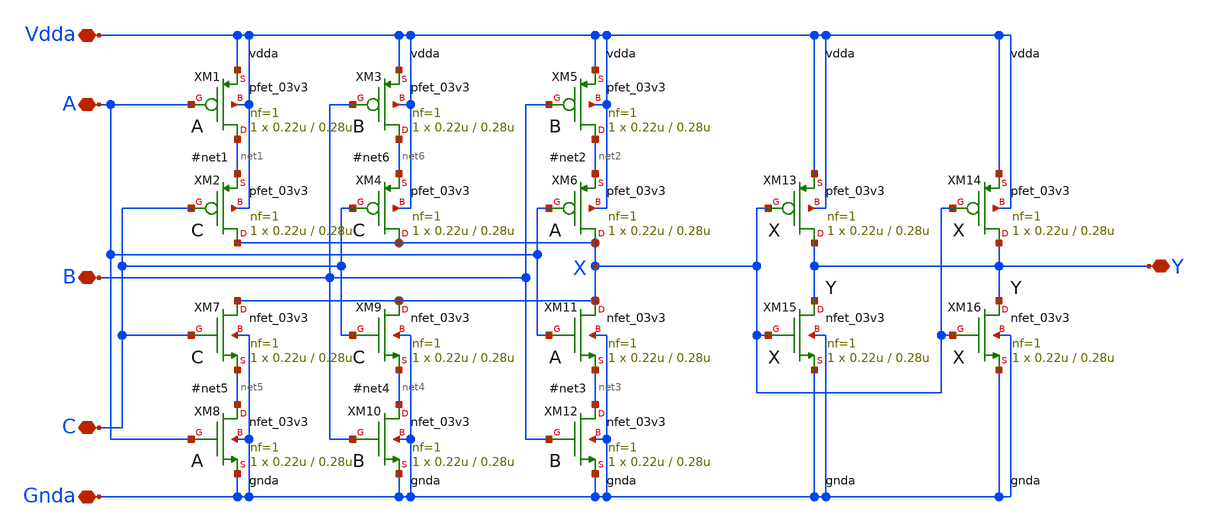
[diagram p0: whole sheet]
** sch_path: xschem/maj3_new.sch
**.subckt maj3_new Vdda Gnda A B C Y
*.iopin Vdda
*.iopin Gnda
*.iopin A
*.iopin B
*.iopin C
*.iopin Y
XM1 net1 A Vdda Vdda pfet_03v3 L=0.28u W=0.22u nf=1 ad='int((nf+1)/2) * W/nf * 0.18u' as='int((nf+2)/2) * W/nf * 0.18u'
+ pd='2*int((nf+1)/2) * (W/nf + 0.18u)' ps='2*int((nf+2)/2) * (W/nf + 0.18u)' nrd='0.18u / W' nrs='0.18u / W'
+ sa=0 sb=0 sd=0 m=1
XM2 X C net1 Vdda pfet_03v3 L=0.28u W=0.22u nf=1 ad='int((nf+1)/2) * W/nf * 0.18u' as='int((nf+2)/2) * W/nf * 0.18u'
+ pd='2*int((nf+1)/2) * (W/nf + 0.18u)' ps='2*int((nf+2)/2) * (W/nf + 0.18u)' nrd='0.18u / W' nrs='0.18u / W'
+ sa=0 sb=0 sd=0 m=1
XM3 net6 B Vdda Vdda pfet_03v3 L=0.28u W=0.22u nf=1 ad='int((nf+1)/2) * W/nf * 0.18u' as='int((nf+2)/2) * W/nf * 0.18u'
+ pd='2*int((nf+1)/2) * (W/nf + 0.18u)' ps='2*int((nf+2)/2) * (W/nf + 0.18u)' nrd='0.18u / W' nrs='0.18u / W'
+ sa=0 sb=0 sd=0 m=1
XM5 net2 B Vdda Vdda pfet_03v3 L=0.28u W=0.22u nf=1 ad='int((nf+1)/2) * W/nf * 0.18u' as='int((nf+2)/2) * W/nf * 0.18u'
+ pd='2*int((nf+1)/2) * (W/nf + 0.18u)' ps='2*int((nf+2)/2) * (W/nf + 0.18u)' nrd='0.18u / W' nrs='0.18u / W'
+ sa=0 sb=0 sd=0 m=1
XM6 X A net2 Vdda pfet_03v3 L=0.28u W=0.22u nf=1 ad='int((nf+1)/2) * W/nf * 0.18u' as='int((nf+2)/2) * W/nf * 0.18u'
+ pd='2*int((nf+1)/2) * (W/nf + 0.18u)' ps='2*int((nf+2)/2) * (W/nf + 0.18u)' nrd='0.18u / W' nrs='0.18u / W'
+ sa=0 sb=0 sd=0 m=1
XM4 X C net6 Vdda pfet_03v3 L=0.28u W=0.22u nf=1 ad='int((nf+1)/2) * W/nf * 0.18u' as='int((nf+2)/2) * W/nf * 0.18u'
+ pd='2*int((nf+1)/2) * (W/nf + 0.18u)' ps='2*int((nf+2)/2) * (W/nf + 0.18u)' nrd='0.18u / W' nrs='0.18u / W'
+ sa=0 sb=0 sd=0 m=1
XM7 X C net5 Gnda nfet_03v3 L=0.28u W=0.22u nf=1 ad='int((nf+1)/2) * W/nf * 0.18u' as='int((nf+2)/2) * W/nf * 0.18u'
+ pd='2*int((nf+1)/2) * (W/nf + 0.18u)' ps='2*int((nf+2)/2) * (W/nf + 0.18u)' nrd='0.18u / W' nrs='0.18u / W'
+ sa=0 sb=0 sd=0 m=1
XM8 net5 A Gnda Gnda nfet_03v3 L=0.28u W=0.22u nf=1 ad='int((nf+1)/2) * W/nf * 0.18u' as='int((nf+2)/2) * W/nf * 0.18u'
+ pd='2*int((nf+1)/2) * (W/nf + 0.18u)' ps='2*int((nf+2)/2) * (W/nf + 0.18u)' nrd='0.18u / W' nrs='0.18u / W'
+ sa=0 sb=0 sd=0 m=1
XM9 X C net4 Gnda nfet_03v3 L=0.28u W=0.22u nf=1 ad='int((nf+1)/2) * W/nf * 0.18u' as='int((nf+2)/2) * W/nf * 0.18u'
+ pd='2*int((nf+1)/2) * (W/nf + 0.18u)' ps='2*int((nf+2)/2) * (W/nf + 0.18u)' nrd='0.18u / W' nrs='0.18u / W'
+ sa=0 sb=0 sd=0 m=1
XM10 net4 B Gnda Gnda nfet_03v3 L=0.28u W=0.22u nf=1 ad='int((nf+1)/2) * W/nf * 0.18u' as='int((nf+2)/2) * W/nf * 0.18u'
+ pd='2*int((nf+1)/2) * (W/nf + 0.18u)' ps='2*int((nf+2)/2) * (W/nf + 0.18u)' nrd='0.18u / W' nrs='0.18u / W'
+ sa=0 sb=0 sd=0 m=1
XM11 X A net3 Gnda nfet_03v3 L=0.28u W=0.22u nf=1 ad='int((nf+1)/2) * W/nf * 0.18u' as='int((nf+2)/2) * W/nf * 0.18u'
+ pd='2*int((nf+1)/2) * (W/nf + 0.18u)' ps='2*int((nf+2)/2) * (W/nf + 0.18u)' nrd='0.18u / W' nrs='0.18u / W'
+ sa=0 sb=0 sd=0 m=1
XM12 net3 B Gnda Gnda nfet_03v3 L=0.28u W=0.22u nf=1 ad='int((nf+1)/2) * W/nf * 0.18u' as='int((nf+2)/2) * W/nf * 0.18u'
+ pd='2*int((nf+1)/2) * (W/nf + 0.18u)' ps='2*int((nf+2)/2) * (W/nf + 0.18u)' nrd='0.18u / W' nrs='0.18u / W'
+ sa=0 sb=0 sd=0 m=1
XM13 Y X Vdda Vdda pfet_03v3 L=0.28u W=0.22u nf=1 ad='int((nf+1)/2) * W/nf * 0.18u' as='int((nf+2)/2) * W/nf * 0.18u'
+ pd='2*int((nf+1)/2) * (W/nf + 0.18u)' ps='2*int((nf+2)/2) * (W/nf + 0.18u)' nrd='0.18u / W' nrs='0.18u / W'
+ sa=0 sb=0 sd=0 m=1
XM14 Y X Vdda Vdda pfet_03v3 L=0.28u W=0.22u nf=1 ad='int((nf+1)/2) * W/nf * 0.18u' as='int((nf+2)/2) * W/nf * 0.18u'
+ pd='2*int((nf+1)/2) * (W/nf + 0.18u)' ps='2*int((nf+2)/2) * (W/nf + 0.18u)' nrd='0.18u / W' nrs='0.18u / W'
+ sa=0 sb=0 sd=0 m=1
XM15 Y X Gnda Gnda nfet_03v3 L=0.28u W=0.22u nf=1 ad='int((nf+1)/2) * W/nf * 0.18u' as='int((nf+2)/2) * W/nf * 0.18u'
+ pd='2*int((nf+1)/2) * (W/nf + 0.18u)' ps='2*int((nf+2)/2) * (W/nf + 0.18u)' nrd='0.18u / W' nrs='0.18u / W'
+ sa=0 sb=0 sd=0 m=1
XM16 Y X Gnda Gnda nfet_03v3 L=0.28u W=0.22u nf=1 ad='int((nf+1)/2) * W/nf * 0.18u' as='int((nf+2)/2) * W/nf * 0.18u'
+ pd='2*int((nf+1)/2) * (W/nf + 0.18u)' ps='2*int((nf+2)/2) * (W/nf + 0.18u)' nrd='0.18u / W' nrs='0.18u / W'
+ sa=0 sb=0 sd=0 m=1
**** begin user architecture code
B
**** end user architecture code
**.ends
.end
